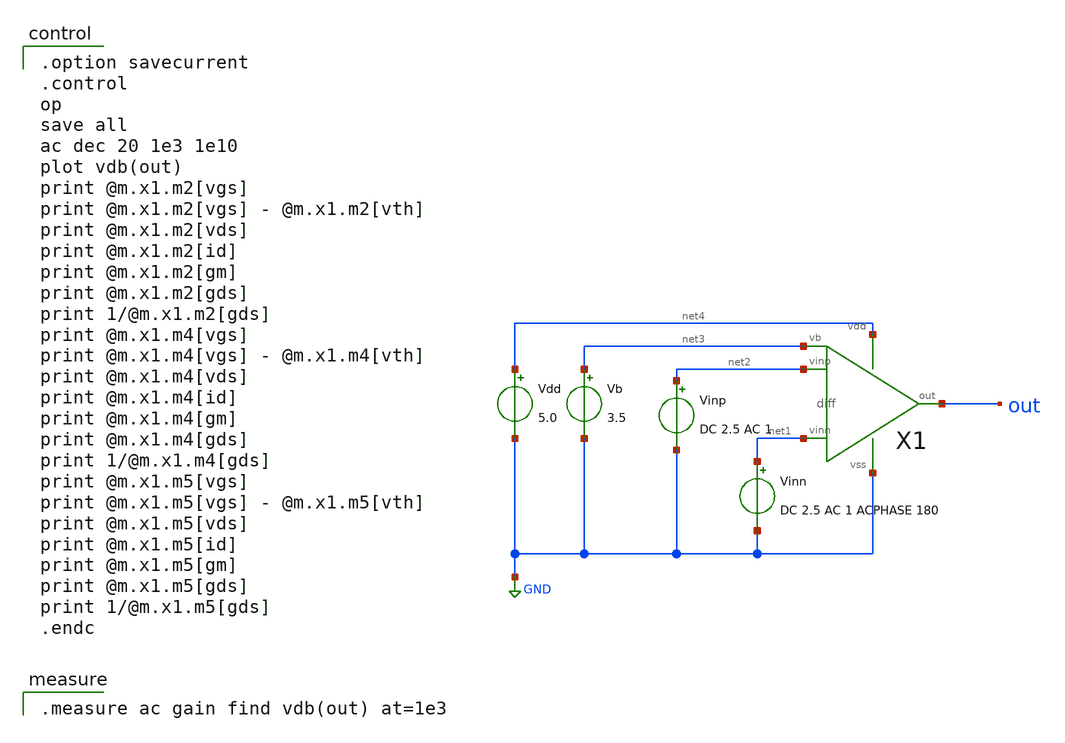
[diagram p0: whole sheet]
** sch_path: OR1/PTC06/opamp/diff-stage_ac.sch
**.subckt diff-stage_ac
Vdd net4 GND 5.0
Vb net3 GND 3.5
Vinn net1 GND DC 2.5 AC 1 ACPHASE 180
Vinp net2 GND DC 2.5 AC 1
X1 net2 net1 out net4 GND net3 diff
**** begin user architecture code

.option savecurrent
.control
op
save all
ac dec 20 1e3 1e10
plot vdb(out)
print @m.x1.m2[vgs]
print @m.x1.m2[vgs] - @m.x1.m2[vth]
print @m.x1.m2[vds]
print @m.x1.m2[id]
print @m.x1.m2[gm]
print @m.x1.m2[gds]
print 1/@m.x1.m2[gds]
print @m.x1.m4[vgs]
print @m.x1.m4[vgs] - @m.x1.m4[vth]
print @m.x1.m4[vds]
print @m.x1.m4[id]
print @m.x1.m4[gm]
print @m.x1.m4[gds]
print 1/@m.x1.m4[gds]
print @m.x1.m5[vgs]
print @m.x1.m5[vgs] - @m.x1.m5[vth]
print @m.x1.m5[vds]
print @m.x1.m5[id]
print @m.x1.m5[gm]
print @m.x1.m5[gds]
print 1/@m.x1.m5[gds]
.endc


.measure ac gain find vdb(out) at=1e3

 .include $::LIB/mos.lib
.include $::LIB/passive.lib
.include $::LIB/diode.lib
**** end user architecture code
**.ends

* expanding   symbol:  diff.sym # of pins=6
** sym_path: diff.sym
** sch_path: diff.sch
.subckt diff vinp vinn out vdd vss vb
*.ipin vinn
*.ipin vinp
*.ipin vb
*.opin out
*.iopin vdd
*.iopin vss
M5 net2 vb vdd vdd pmos L=2u W=40u m=1
M1 net1 vinn net2 net2 pmos L=2u W=200u m=1
M2 out vinp net2 net2 pmos L=2u W=200u m=1
M3 net1 net1 vss vss nmos L=2u W=10u m=1
M4 out net1 vss vss nmos L=2u W=10u m=1
.ends

.GLOBAL GND
.end
